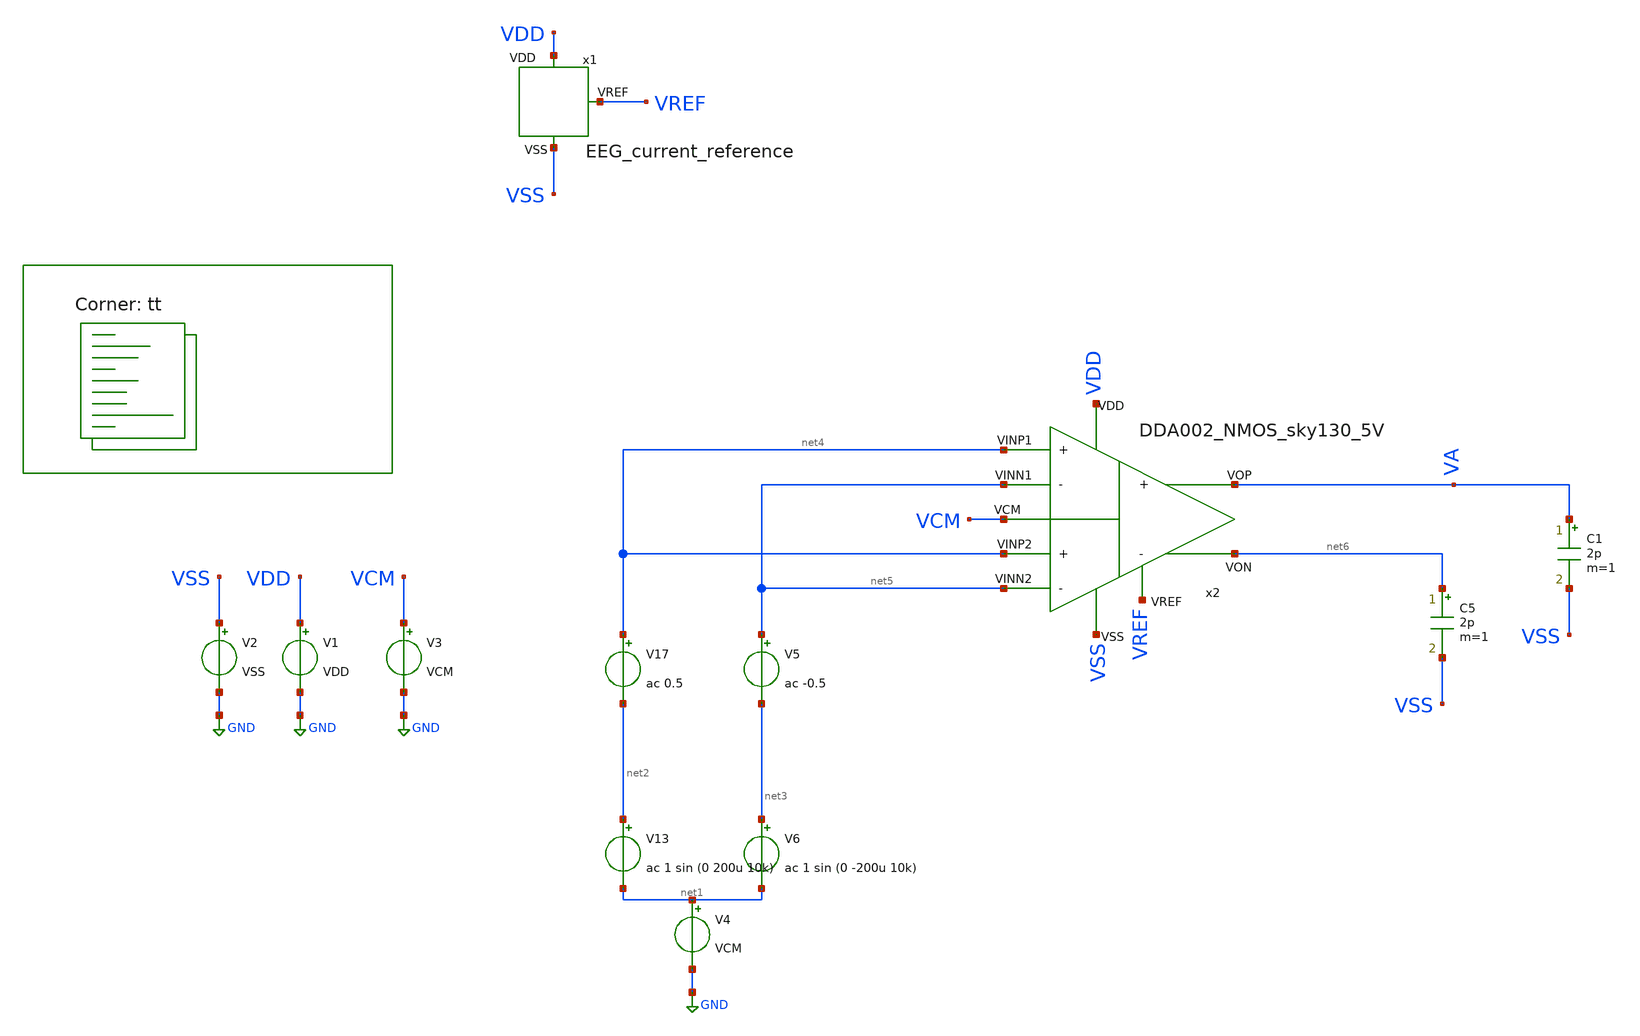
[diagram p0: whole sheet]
** sch_path: Learning/complex_projects/A_Two-Stage_Time_Division_Multiplexing_AFE_with_Input_Impedance_Boosting_DDA_for_EEG_Signal_Acquisition/sky130A_5V/input_buffer_chopper/DDA_TB.sch
**.subckt DDA_TB
V1 VDD GND VDD
V2 VSS GND VSS
x1 VDD VSS VREF EEG_current_reference
x2 VDD VSS VREF net5 net5 net4 net4 VCM VA net6 DDA002_NMOS_sky130_5V
V3 VCM GND VCM
V4 net1 GND VCM
V17 net4 net2 ac 0.5
V5 net5 net3 ac -0.5
C5 net6 VSS 2p m=1
C1 VA VSS 2p m=1
V13 net2 net1 ac 1 sin (0 200u 10k)
V6 net3 net1 ac 1 sin (0 -200u 10k)
**** begin user architecture code
.lib $::SKYWATER_MODELS/sky130.lib.spice tt

.Temp -40
.param VDD = 5
.param VSS = 0
.param CL = 3p
.param V_OFF = -400u
.param VCM = 2.5


.control

	save all
	ac dec 100 1 10G
	plot db(v(VA)) (180+(180*ph(v(VA))/pi))
	op
	print v(VA)
	print (5*-I(V1))
	tran 10n 500u
        plot v(VA)


.endc




**** end user architecture code
**.ends
.GLOBAL GND
.end
